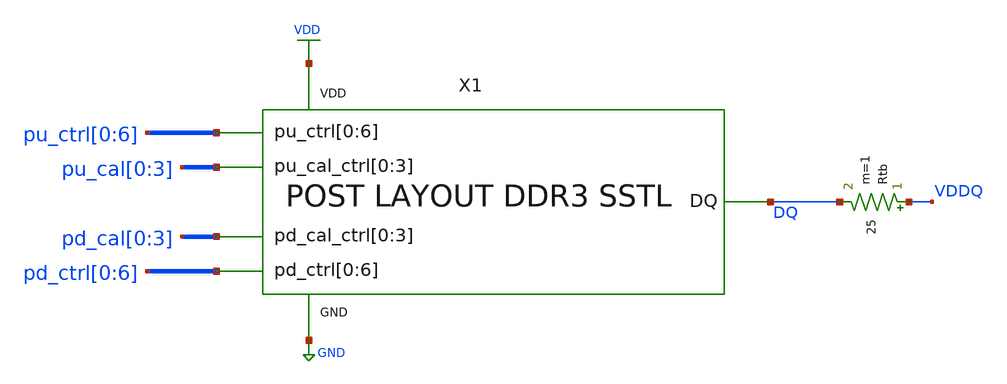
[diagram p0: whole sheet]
** sch_path: schem/post_layout_sstl_cap_tb.sch
* Copyright 2021 Stefan Frederik Schippers
* Licensed under the Apache License, Version 2.0 (the "License");
* you may not use this file except in compliance with the License.
* You may obtain a copy of the License at
* https://www.apache.org/licenses/LICENSE-2.0
* Unless required by applicable law or agreed to in writing, software
* distributed under the License is distributed on an "AS IS" BASIS,
* WITHOUT WARRANTIES OR CONDITIONS OF ANY KIND, either express or implied.
* See the License for the specific language governing permissions and
* limitations under the License.
**.subckt post_layout_sstl_cap_tb
Rtb VDDQ DQ 25 m=1
X1 DQ GND pd_cal[0] pd_cal[1] pd_cal[2] pd_cal[3] pd_ctrl[0] pd_ctrl[1] pd_ctrl[2] pd_ctrl[3]
+ pd_ctrl[4] pd_ctrl[5] pd_ctrl[6] pu_cal[0] pu_cal[1] pu_cal[2] pu_cal[3] pu_ctrl[0] pu_ctrl[1] pu_ctrl[2]
+ pu_ctrl[3] pu_ctrl[4] pu_ctrl[5] pu_ctrl[6] VDD SSTL
**** begin user architecture code
 ** Local library links to pdk
.lib ./sky130/libs/SED_process_SED_lib.spice SED_process_SED
.include $::SKYWATER_STDCELLS/sky130_fd_sc_hd.spice
.include ./layout/pex_SSTL.spice

**** end user architecture code
**.ends
.GLOBAL GND
.GLOBAL VDD
**** begin user architecture code


* power voltage
vvdd VDD 0 SED_vdd_SED

** LEG CONTROL **
vpu_ctrl0 pu_ctrl[0] 0 SED_puctrl0_SED
vpu_ctrl1 pu_ctrl[1] 0 SED_puctrl1_SED
vpu_ctrl2 pu_ctrl[2] 0 SED_puctrl2_SED
vpu_ctrl3 pu_ctrl[3] 0 SED_puctrl3_SED
vpu_ctrl4 pu_ctrl[4] 0 SED_puctrl4_SED
vpu_ctrl5 pu_ctrl[5] 0 SED_puctrl5_SED
vpu_ctrl6 pu_ctrl[6] 0 SED_puctrl6_SED
* PULLDOWN
vpd_ctrl0 pd_ctrl[0] 0 SED_pdctrl0_SED
vpd_ctrl1 pd_ctrl[1] 0 SED_pdctrl1_SED
vpd_ctrl2 pd_ctrl[2] 0 SED_pdctrl2_SED
vpd_ctrl3 pd_ctrl[3] 0 SED_pdctrl3_SED
vpd_ctrl4 pd_ctrl[4] 0 SED_pdctrl4_SED
vpd_ctrl5 pd_ctrl[5] 0 SED_pdctrl5_SED
vpd_ctrl6 pd_ctrl[6] 0 SED_pdctrl6_SED

** CALIBRATION CONTROL **
* PULLUP
vpu_cal0 pu_cal[0] 0 SED_pucal0_SED
vpu_cal1 pu_cal[1] 0 SED_pucal1_SED
vpu_cal2 pu_cal[2] 0 SED_pucal2_SED
vpu_cal3 pu_cal[3] 0 SED_pucal3_SED
* PULLDOWN
vpd_cal0 pd_cal[0] 0 SED_pdcal0_SED
vpd_cal1 pd_cal[1] 0 SED_pdcal1_SED
vpd_cal2 pd_cal[2] 0 SED_pdcal2_SED
vpd_cal3 pd_cal[3] 0 SED_pdcal3_SED

* INPUT SIGNAL
*                vlow,       vhigh, delay, risetime, falltime, pulsewidth, period, phase
vvddq vddq 0 0 PULSE 0 SED_vdd_SED  0.25n  10p       10p       2n          4n      0

.control
save all
set temp=SED_temp_SED
set num_threads=6

* RUN SIMULATION
tran 1p 4.25n
* Measure rise time
meas tran tdiff_charge    trig at=0.25n targ dq val=SED_vih_SED rise=1
* Measure fall time
meas tran tdiff_discharge trig at=2.25n targ dq val=SED_vil_SED fall=1

* OUTPUT
wrdata ./out/SED_plotName_SED/SED_plotName_SED.txt tdiff_charge tdiff_discharge
set hcopydevtype = svg
hardcopy ./out/SED_plotName_SED/SED_plotName_SED.svg dq vddq title 'DQ vs time'

.endc


**** end user architecture code
.end
